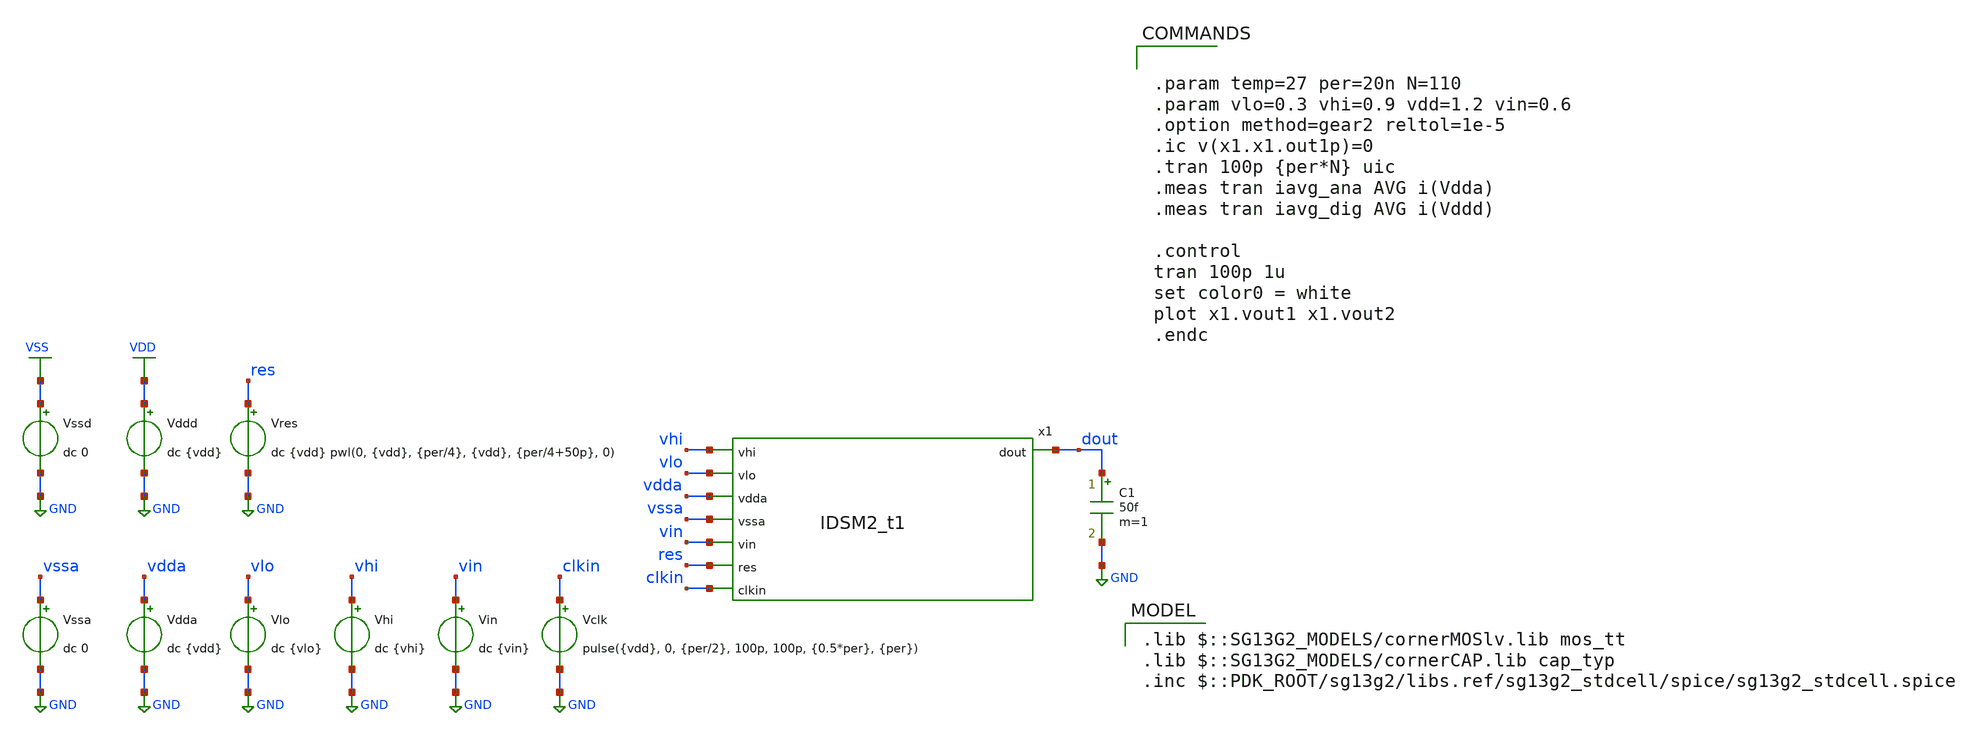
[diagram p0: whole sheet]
** sch_path: schematics/tb_IDSM2oldtetest.sch
**.subckt tb_IDSM2oldtetest
Vddd VDD GND dc {vdd}
Vssd VSS GND dc 0
Vres res GND dc {vdd} pwl(0, {vdd}, {per/4}, {vdd}, {per/4+50p}, 0)
Vssa vssa GND dc 0
Vdda vdda GND dc {vdd}
Vlo vlo GND dc {vlo}
Vhi vhi GND dc {vhi}
Vin vin GND dc {vin}
Vclk clkin GND pulse({vdd}, 0, {per/2}, 100p, 100p, {0.5*per}, {per})
C1 dout GND 50f m=1
x1 vhi vlo vdda vssa vin dout res clkin IDSM2_t1
**** begin user architecture code


.param temp=27 per=20n N=110
.param vlo=0.3 vhi=0.9 vdd=1.2 vin=0.6
.option method=gear2 reltol=1e-5
.ic v(x1.x1.out1p)=0
.tran 100p {per*N} uic
.meas tran iavg_ana AVG i(Vdda)
.meas tran iavg_dig AVG i(Vddd)

.control
tran 100p 1u
set color0 = white
plot x1.vout1 x1.vout2
.endc


 .lib $::SG13G2_MODELS/cornerMOSlv.lib mos_tt
.lib $::SG13G2_MODELS/cornerCAP.lib cap_typ
.inc $::PDK_ROOT/sg13g2/libs.ref/sg13g2_stdcell/spice/sg13g2_stdcell.spice

**** end user architecture code
**.ends
.GLOBAL VDD
.GLOBAL GND
.GLOBAL VSS
.end
